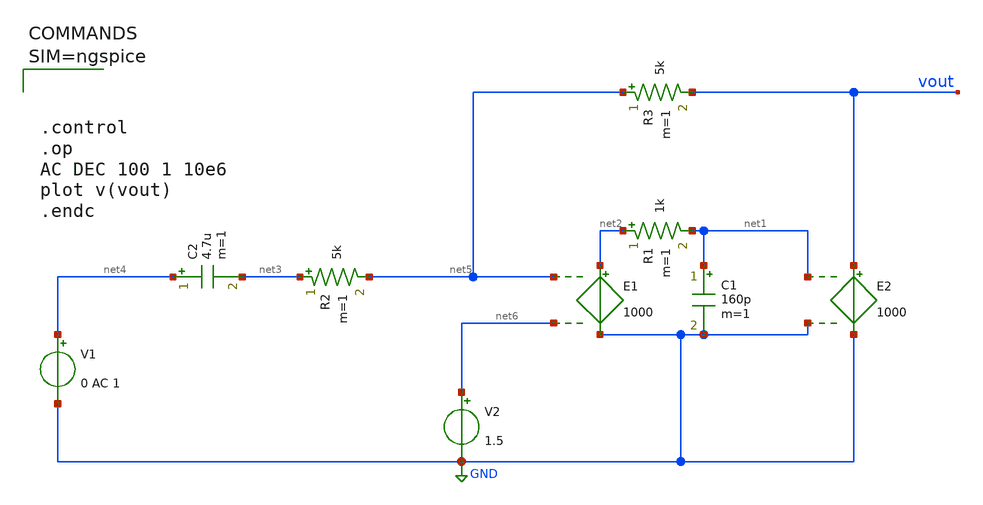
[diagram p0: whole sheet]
** sch_path: xschem/mictest_buffer.sch
**.subckt mictest_buffer
E1 net2 GND net5 net6 1000
E2 vout GND net1 GND 1000
C1 net1 GND 160p m=1
R1 net2 net1 1k m=1
R2 net3 net5 5k m=1
R3 net5 vout 5k m=1
C2 net4 net3 4.7u m=1
V1 net4 GND 0 AC 1
V2 net6 GND 1.5
**** begin user architecture code




.control
.op
AC DEC 100 1 10e6
plot v(vout)
.endc



**** end user architecture code
**.ends
.GLOBAL GND
.end
